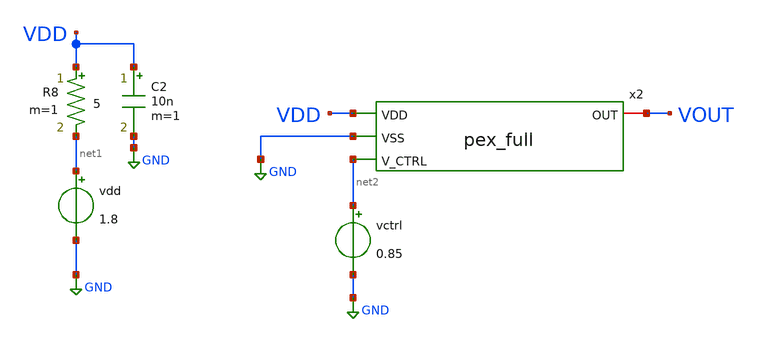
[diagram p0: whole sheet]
** sch_path: schem/corner_full_tb.sch
**.subckt corner_full_tb
vdd net1 GND 1.8
C2 VDD GND 10n m=1
R8 VDD net1 5 m=1
vctrl net2 GND 0.85
x2 VDD GND VOUT net2 vco_pex
**** begin user architecture code



.include /home/zhixuan/projects/fyp_vco/magic/full/vco_pex.spice
.lib /usr/local/share/pdk/sky130A/libs.tech/ngspice/sky130.lib.spice ff

.tran 0.1n 2u
.save all

.control
    run

    meas tran t11 when VOUT=0.9 rise=2
    meas tran t21 when VOUT=0.9 rise=3

    * Calculate period and frequency from 2nd period onwards
    let period1 = t21 - t11

    let freq1 = 1 / period1

    meas tran idd1 avg i(vdd) from=t11 to=2u
    let idd1 = abs(idd1)

    plot VOUT

    print period1
    print freq1
    print idd1

    * echo "VOUT2 v(x2.comp_p_0/VIN_N)" > /home/zhixuan/projects/fyp_vco/schem/full_out1.txt
    * print col VOUT2 v(x2.comp_p_0/VIN_N) >> /home/zhixuan/projects/fyp_vco/schem/full_out1.txt
.endc

.end


**** end user architecture code
**.ends
.GLOBAL GND
.end
